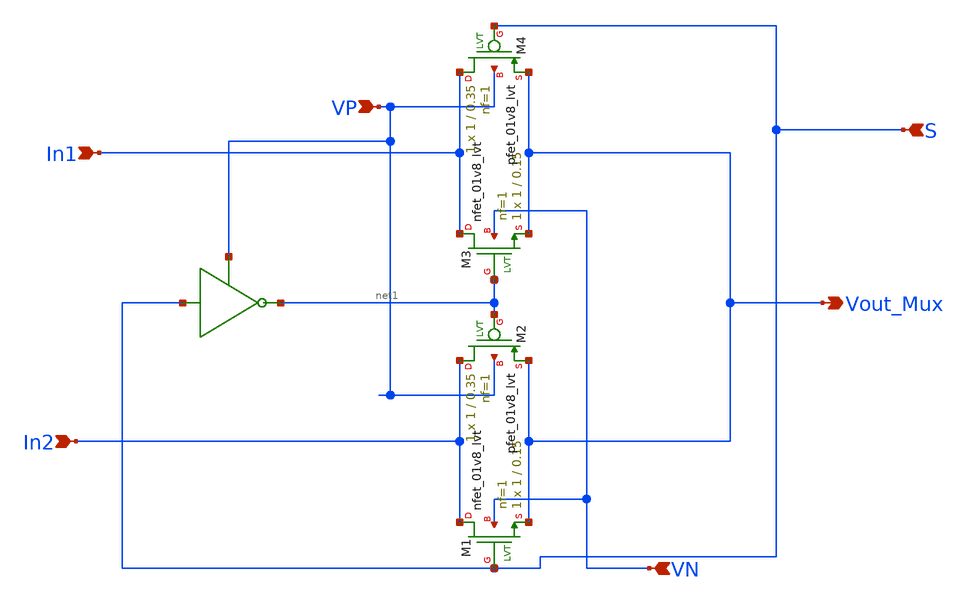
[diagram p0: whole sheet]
** sch_path: Current Sensor/mux21.sch
**.subckt mux21 VP Vout_Mux S In1 In2 VN
*.ipin VP
*.opin Vout_Mux
*.ipin S
*.ipin In1
*.ipin In2
*.ipin VN
XM1 In2 S Vout_Mux VN sky130_fd_pr__nfet_01v8_lvt L=0.15 W=1 nf=1 ad='int((nf+1)/2) * W/nf * 0.29' as='int((nf+2)/2) * W/nf * 0.29'
+ pd='2*int((nf+1)/2) * (W/nf + 0.29)' ps='2*int((nf+2)/2) * (W/nf + 0.29)' nrd='0.29 / W' nrs='0.29 / W'
+ sa=0 sb=0 sd=0 mult=1 m=1
XM2 In2 net1 Vout_Mux VP sky130_fd_pr__pfet_01v8_lvt L=0.35 W=1 nf=1 ad='int((nf+1)/2) * W/nf * 0.29'
+ as='int((nf+2)/2) * W/nf * 0.29' pd='2*int((nf+1)/2) * (W/nf + 0.29)' ps='2*int((nf+2)/2) * (W/nf + 0.29)'
+ nrd='0.29 / W' nrs='0.29 / W' sa=0 sb=0 sd=0 mult=1 m=1
XM3 In1 net1 Vout_Mux VN sky130_fd_pr__nfet_01v8_lvt L=0.15 W=1 nf=1 ad='int((nf+1)/2) * W/nf * 0.29'
+ as='int((nf+2)/2) * W/nf * 0.29' pd='2*int((nf+1)/2) * (W/nf + 0.29)' ps='2*int((nf+2)/2) * (W/nf + 0.29)'
+ nrd='0.29 / W' nrs='0.29 / W' sa=0 sb=0 sd=0 mult=1 m=1
XM4 In1 S Vout_Mux VP sky130_fd_pr__pfet_01v8_lvt L=0.35 W=1 nf=1 ad='int((nf+1)/2) * W/nf * 0.29' as='int((nf+2)/2) * W/nf * 0.29'
+ pd='2*int((nf+1)/2) * (W/nf + 0.29)' ps='2*int((nf+2)/2) * (W/nf + 0.29)' nrd='0.29 / W' nrs='0.29 / W'
+ sa=0 sb=0 sd=0 mult=1 m=1
**.ends
.end
